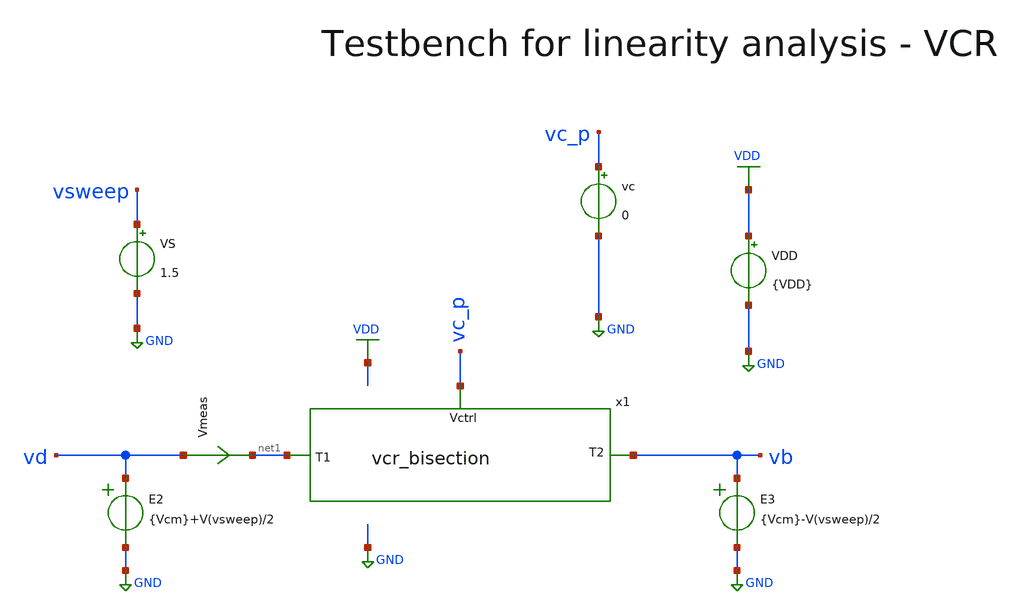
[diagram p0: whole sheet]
** sch_path: macros/heichips26_vcr/macros/vcr_bisection/testbenches/xschem/res_tb_linearity_vctrl.sch
**.subckt res_tb_linearity_vctrl
VDD VDD GND {VDD}
VS vsweep GND 1.5
Vmeas vd net1 0
.save i(vmeas)
E2 vd GND VOL=' {Vcm}+V(vsweep)/2 '
E3 vb GND VOL=' {Vcm}-V(vsweep)/2 '
vc vc_p GND 0
x1 vc_p net1 vb vcr_bisection
**** begin user architecture code

.lib cornerMOSlv.lib mos_tt
.lib cornerMOShv.lib mos_tt
.lib cornerRES.lib res_typ
.lib cornerDIO.lib dio_tt
.lib cornerCAP.lib cap_typ



* .include ../../../netlist/pex/inverter_magic_pex_3.spice
.param VDD=3.3
.csparam VDD=VDD
.param Vcm=2
.csparam Vcm=Vcm
.param temp=27
.options savecurrents klu method=gear reltol=1e-3 abstol=1e-15 gmin=1e-15 rshunt=1e13
.control
let vcc = 0.75

save all
set appendwrite



repeat 5
  alter vc $&vcc

  * DC Sweep
  dc VS -1 1 1m
  remzerovec
  let vcc = vcc + 0.25
end
write @schname\.raw
set appendwrite

* Plotting
plot (dc1.v(vd) - dc1.v(vb))/(dc1.i(vmeas)) (dc2.v(vd) - dc2.v(vb))/(dc2.i(vmeas)) (dc3.v(vd) -
+ dc3.v(vb))/(dc3.i(vmeas)) (dc4.v(vd) - dc4.v(vb))/(dc4.i(vmeas)) (dc5.v(vd) - dc5.v(vb))/(dc5.i(vmeas)) ylimit 0 10k

plot dc1.i(vmeas) dc2.i(vmeas) dc3.i(vmeas) dc4.i(vmeas) dc5.i(vmeas)

* Write Data
unset appendwrite
set wr_vecnames
set wr_singlescale
wrdata ../plot_simulations/data/@schname\.txt v(vc_p) dc1.v(vsweep)/(dc1.i(Vmeas))
+ dc2.v(vsweep)/(dc2.i(Vmeas)) dc3.v(vsweep)/(dc3.i(Vmeas)) dc4.v(vsweep)/(dc4.i(Vmeas)) dc5.v(vsweep)/(dc5.i(Vmeas))

write res_tb_linearity.raw

*quit
.endc


**** end user architecture code
**.ends

* expanding   symbol:  vcr_bisection.sym # of pins=3
** sym_path: macros/heichips26_analog_project/macros/vcr_bisection/schematic/xschem/vcr_bisection.sym
** sch_path: macros/heichips26_analog_project/macros/vcr_bisection/schematic/xschem/vcr_bisection.sch
.subckt vcr_bisection Vctrl T1 T2
*.ipin T1
*.ipin T2
*.ipin Vctrl
R1 vcm T1 10k m=1
R2 T2 vcm 10k m=1
Vmeas T1 net1 0
.save i(vmeas)
XM1 net1 Vctrl T2 vcm sg13_hv_pmos w=50u l=10u ng=10 m=1 mm_ok=1
.ends

.GLOBAL GND
.GLOBAL VDD
.end
